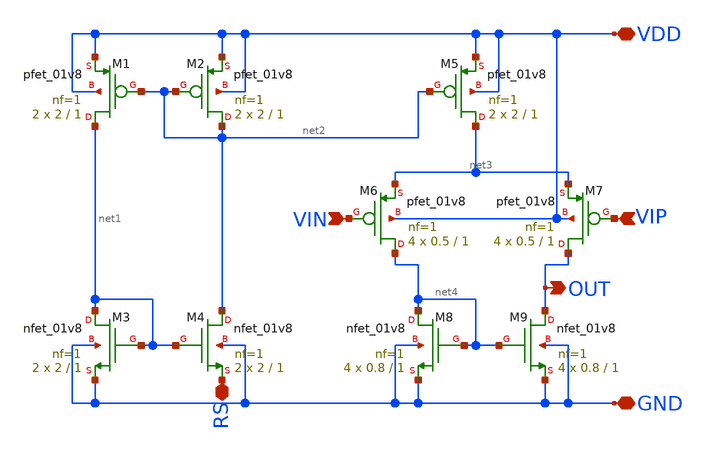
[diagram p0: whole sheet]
** sch_path: opamp1/xschem/opamp1.sch
**.subckt opamp1 VDD GND RS VIN VIP OUT
*.iopin VDD
*.iopin GND
*.iopin RS
*.ipin VIN
*.ipin VIP
*.opin OUT
XM4 net2 net1 RS GND sky130_fd_pr__nfet_01v8 L=1 W=2 nf=1 ad='int((nf+1)/2) * W/nf * 0.29' as='int((nf+2)/2) * W/nf * 0.29'
+ pd='2*int((nf+1)/2) * (W/nf + 0.29)' ps='2*int((nf+2)/2) * (W/nf + 0.29)' nrd='0.29 / W' nrs='0.29 / W'
+ sa=0 sb=0 sd=0 mult=2 m=2
XM3 net1 net1 GND GND sky130_fd_pr__nfet_01v8 L=1 W=2 nf=1 ad='int((nf+1)/2) * W/nf * 0.29' as='int((nf+2)/2) * W/nf * 0.29'
+ pd='2*int((nf+1)/2) * (W/nf + 0.29)' ps='2*int((nf+2)/2) * (W/nf + 0.29)' nrd='0.29 / W' nrs='0.29 / W'
+ sa=0 sb=0 sd=0 mult=2 m=2
XM8 net4 net4 GND GND sky130_fd_pr__nfet_01v8 L=1 W=0.8 nf=1 ad='int((nf+1)/2) * W/nf * 0.29' as='int((nf+2)/2) * W/nf * 0.29'
+ pd='2*int((nf+1)/2) * (W/nf + 0.29)' ps='2*int((nf+2)/2) * (W/nf + 0.29)' nrd='0.29 / W' nrs='0.29 / W'
+ sa=0 sb=0 sd=0 mult=4 m=4
XM9 OUT net4 GND GND sky130_fd_pr__nfet_01v8 L=1 W=0.8 nf=1 ad='int((nf+1)/2) * W/nf * 0.29' as='int((nf+2)/2) * W/nf * 0.29'
+ pd='2*int((nf+1)/2) * (W/nf + 0.29)' ps='2*int((nf+2)/2) * (W/nf + 0.29)' nrd='0.29 / W' nrs='0.29 / W'
+ sa=0 sb=0 sd=0 mult=4 m=4
XM6 net4 VIN net3 VDD sky130_fd_pr__pfet_01v8 L=1 W=0.5 nf=1 ad='int((nf+1)/2) * W/nf * 0.29' as='int((nf+2)/2) * W/nf * 0.29'
+ pd='2*int((nf+1)/2) * (W/nf + 0.29)' ps='2*int((nf+2)/2) * (W/nf + 0.29)' nrd='0.29 / W' nrs='0.29 / W'
+ sa=0 sb=0 sd=0 mult=4 m=4
XM7 OUT VIP net3 VDD sky130_fd_pr__pfet_01v8 L=1 W=0.5 nf=1 ad='int((nf+1)/2) * W/nf * 0.29' as='int((nf+2)/2) * W/nf * 0.29'
+ pd='2*int((nf+1)/2) * (W/nf + 0.29)' ps='2*int((nf+2)/2) * (W/nf + 0.29)' nrd='0.29 / W' nrs='0.29 / W'
+ sa=0 sb=0 sd=0 mult=4 m=4
XM5 net3 net2 VDD VDD sky130_fd_pr__pfet_01v8 L=1 W=2 nf=1 ad='int((nf+1)/2) * W/nf * 0.29' as='int((nf+2)/2) * W/nf * 0.29'
+ pd='2*int((nf+1)/2) * (W/nf + 0.29)' ps='2*int((nf+2)/2) * (W/nf + 0.29)' nrd='0.29 / W' nrs='0.29 / W'
+ sa=0 sb=0 sd=0 mult=2 m=2
XM1 net1 net2 VDD VDD sky130_fd_pr__pfet_01v8 L=1 W=2 nf=1 ad='int((nf+1)/2) * W/nf * 0.29' as='int((nf+2)/2) * W/nf * 0.29'
+ pd='2*int((nf+1)/2) * (W/nf + 0.29)' ps='2*int((nf+2)/2) * (W/nf + 0.29)' nrd='0.29 / W' nrs='0.29 / W'
+ sa=0 sb=0 sd=0 mult=2 m=2
XM2 net2 net2 VDD VDD sky130_fd_pr__pfet_01v8 L=1 W=2 nf=1 ad='int((nf+1)/2) * W/nf * 0.29' as='int((nf+2)/2) * W/nf * 0.29'
+ pd='2*int((nf+1)/2) * (W/nf + 0.29)' ps='2*int((nf+2)/2) * (W/nf + 0.29)' nrd='0.29 / W' nrs='0.29 / W'
+ sa=0 sb=0 sd=0 mult=2 m=2
**.ends
.end
